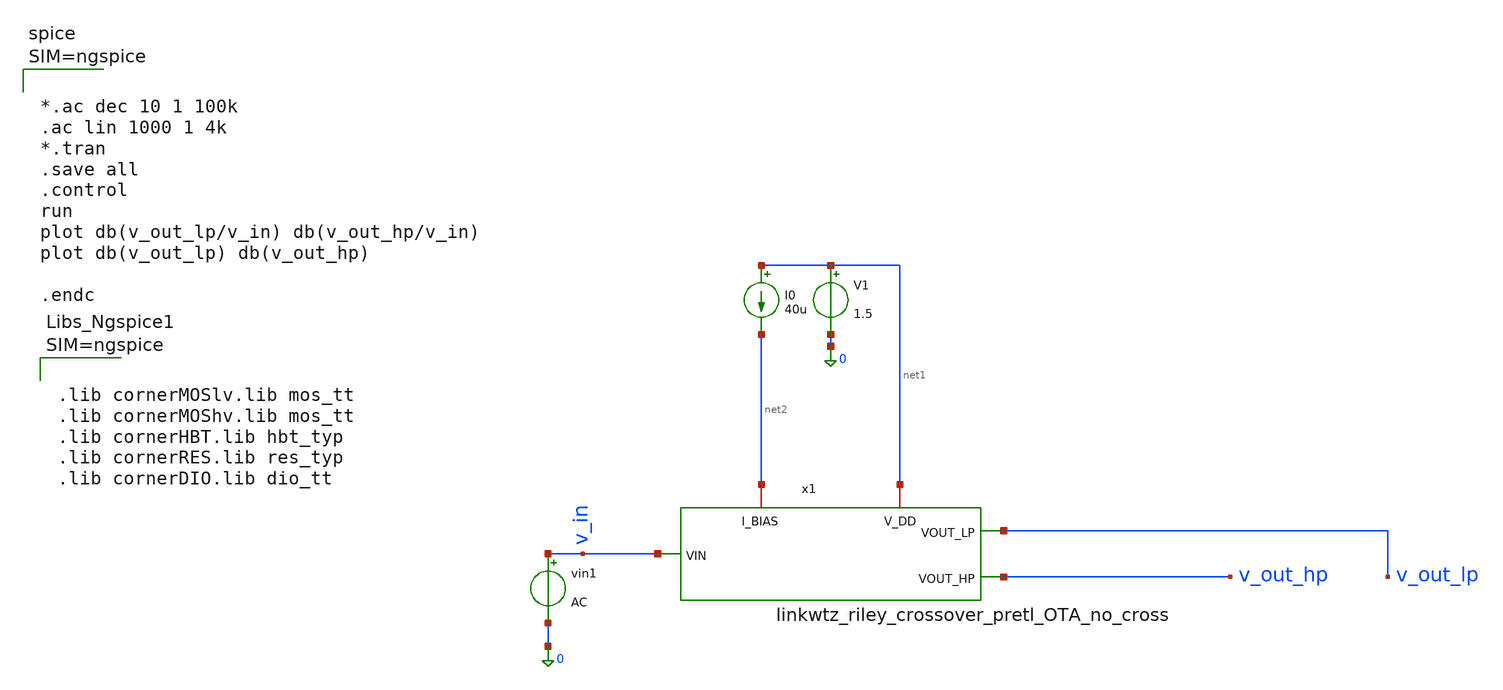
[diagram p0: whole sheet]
** sch_path: 004_Real_Circuits/linkwitz_riley_real_circuit_pretl_no_cross_top_tb.sch
* 004_Real_Circuits/ota-5t.sch:
* (c) 2024-2025 Harald Pretl, Apache-2.0 license
**.subckt linkwitz_riley_real_circuit_pretl_no_cross_top_tb
I0 net1 net2 40u
V1 net1 0 1.5
vin1 v_in 0 AC
x1 net1 net2 v_out_lp v_in v_out_hp linkwtz_riley_crossover_pretl_OTA_no_cross
**** begin user architecture code



.lib cornerMOSlv.lib mos_tt
.lib cornerMOShv.lib mos_tt
.lib cornerHBT.lib hbt_typ
.lib cornerRES.lib res_typ
.lib cornerDIO.lib dio_tt






*.ac dec 10 1 100k
.ac lin 1000 1 4k
*.tran
.save all
.control
run
plot db(v_out_lp/v_in) db(v_out_hp/v_in)
plot db(v_out_lp) db(v_out_hp)

.endc



**** end user architecture code
**.ends

* expanding   symbol:
*+  /foss/designs/GitHub_Repo/004_Real_Circuits/linkwtz_riley_crossover_pretl_OTA_no_cross.sym # of pins=5
** sym_path: 004_Real_Circuits/linkwtz_riley_crossover_pretl_OTA_no_cross.sym
** sch_path: 004_Real_Circuits/linkwtz_riley_crossover_pretl_OTA_no_cross.sch
.subckt linkwtz_riley_crossover_pretl_OTA_no_cross V_DD I_BIAS VOUT_LP VIN VOUT_HP
*.opin VOUT_LP
*.opin VOUT_HP
*.ipin VIN
*.iopin I_BIAS
*.iopin V_DD
R1 net1 VIN R_LP m=1
.param C_LP=1.06e-6
.param R_LP=1000
.param C_HP=50e-9
.param R_HP=21220
.param R_IN=1k
R2 net3 net1 R_LP m=1
C1 net3 0 C_LP m=1
C2 net1 net2 C_LP m=1
C3 VIN net5 C_HP m=1
C4 net5 net6 C_HP m=1
R3 net5 net4 R_HP m=1
R4 net6 0 R_HP m=1
C5 VOUT_LP net2 50f m=1
C6 VOUT_HP net4 50f m=1
x1 V_DD net2 net3 net2 I_BIAS V_DD 0 ota-5t
x2 V_DD net4 net6 net4 I_BIAS V_DD 0 ota-5t
.ends


* expanding   symbol:  /foss/designs/GitHub_Repo/004_Real_Circuits/ota-5t.sym # of pins=7
** sym_path: /foss/designs/GitHub_Repo/004_Real_Circuits/ota-5t.sym
** sch_path: /foss/designs/GitHub_Repo/004_Real_Circuits/ota-5t.sch
.subckt ota-5t vdd vout vinp vinn ibias_20u d_ena vss
*.ipin ibias_20u
*.iopin vdd
*.iopin vss
*.ipin vinp
*.ipin vinn
*.opin vout
*.ipin d_ena
XM5 tail gate_n vss vss sg13_lv_nmos w=1.0u l=5u ng=1 m=1 mm_ok=1
XM4 vout gate_p vdd vdd sg13_lv_pmos w=2.5u l=5u ng=1 m=1 mm_ok=1
XM1 gate_p vinp tail vss sg13_lv_nmos w=2u l=5u ng=1 m=1 mm_ok=1
XM2 vout vinn tail vss sg13_lv_nmos w=2u l=5u ng=1 m=1 mm_ok=1
XM3 gate_p gate_p vdd vdd sg13_lv_pmos w=2.5u l=5u ng=1 m=1 mm_ok=1
XM6 ibias_20u gate_n vss vss sg13_lv_nmos w=6.5u l=5u ng=5 m=1 mm_ok=1
XM9 gate_n ena_n vss vss sg13_lv_nmos w=0.5u l=0.13u ng=1 m=1 mm_ok=1
XM11 gate_p ena vdd vdd sg13_lv_pmos w=1.5u l=0.13u ng=1 m=1 mm_ok=1
XM7 ena ena_n vss vss sg13_lv_nmos w=0.5u l=0.13u ng=1 m=1 mm_ok=1
XM8 ena ena_n vdd vdd sg13_lv_pmos w=1.5u l=0.13u ng=1 m=1 mm_ok=1
XM10 ibias_20u ena gate_n vss sg13_lv_nmos w=0.5u l=0.13u ng=1 m=1 mm_ok=1
XM12 ena_n d_ena vss vss sg13_lv_nmos w=0.5u l=0.13u ng=1 m=1 mm_ok=1
XM13 ena_n d_ena vdd vdd sg13_lv_pmos w=1.5u l=0.13u ng=1 m=1 mm_ok=1
.ends

.end
